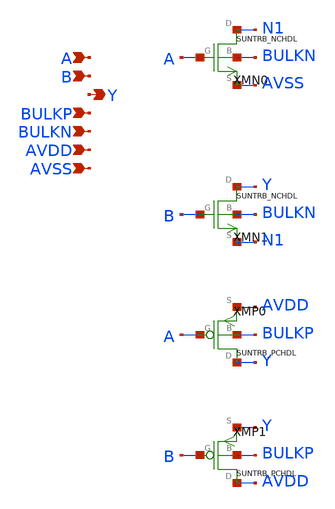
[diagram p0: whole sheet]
** sch_path: ip/sun_trb_sky130nm/design/SUN_TRB_SKY130NM/SUNTRB_NDX1_CV.sch
**.subckt SUNTRB_NDX1_CV A B Y BULKP BULKN AVDD AVSS
*.ipin A
*.ipin B
*.opin Y
*.ipin BULKP
*.ipin BULKN
*.ipin AVDD
*.ipin AVSS
XMN0 N1 A AVSS BULKN SUNTRB_NCHDL xoffset=0 yoffset=0 angle=0
XMN1 Y B N1 BULKN SUNTRB_NCHDL xoffset=0 yoffset=0 angle=0
XMP0 Y A AVDD BULKP SUNTRB_PCHDL xoffset=0 yoffset=0 angle=0
XMP1 AVDD B Y BULKP SUNTRB_PCHDL xoffset=0 yoffset=0 angle=0
**.ends
.end
